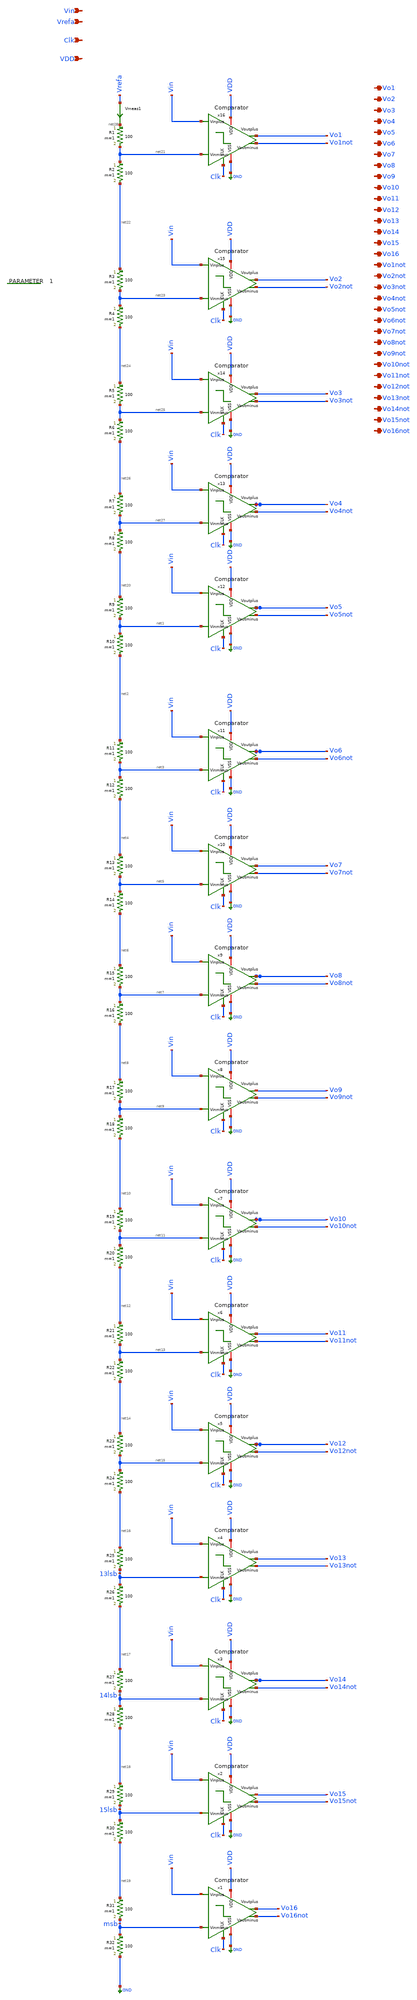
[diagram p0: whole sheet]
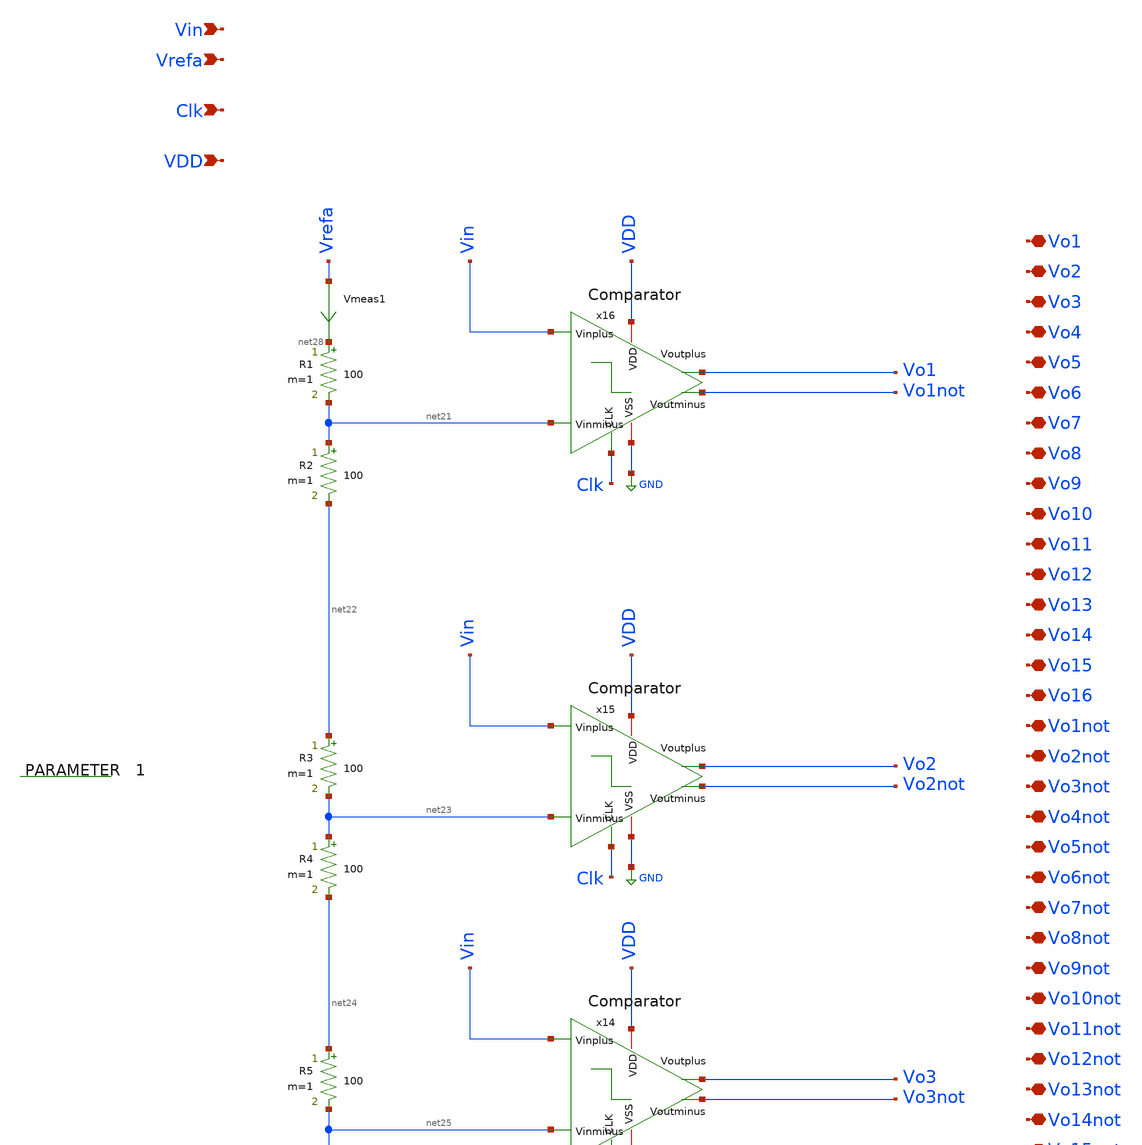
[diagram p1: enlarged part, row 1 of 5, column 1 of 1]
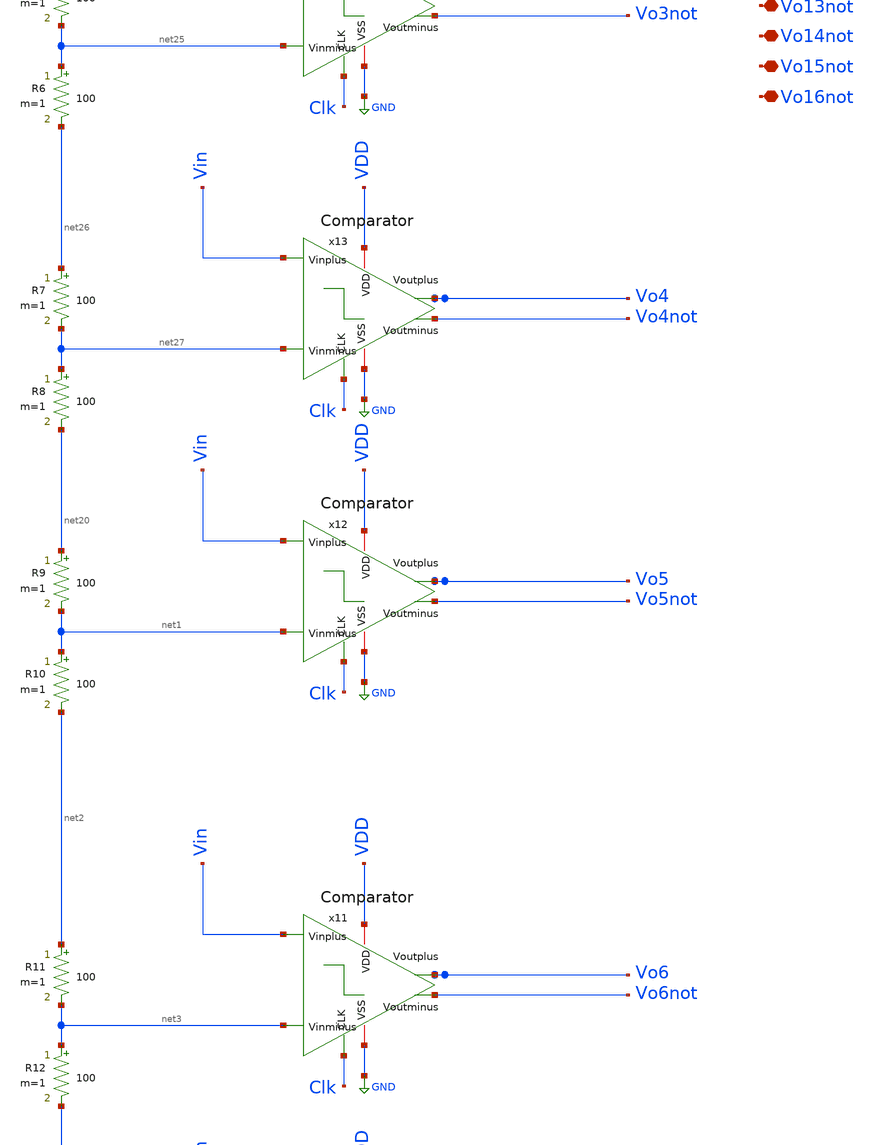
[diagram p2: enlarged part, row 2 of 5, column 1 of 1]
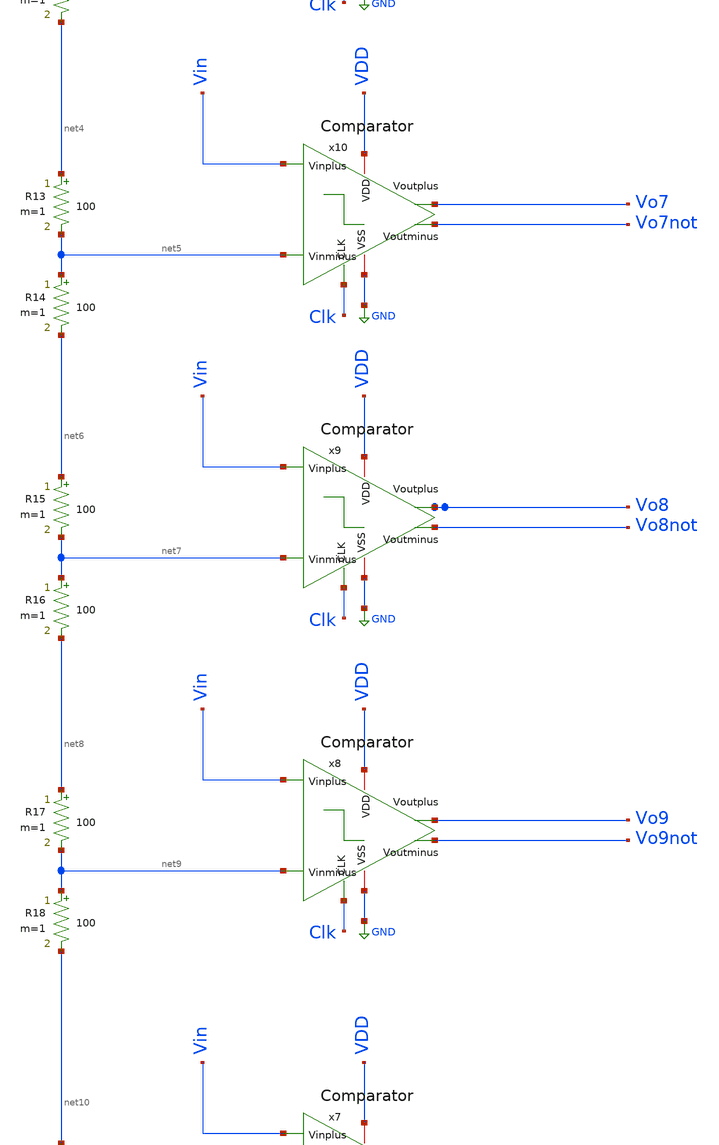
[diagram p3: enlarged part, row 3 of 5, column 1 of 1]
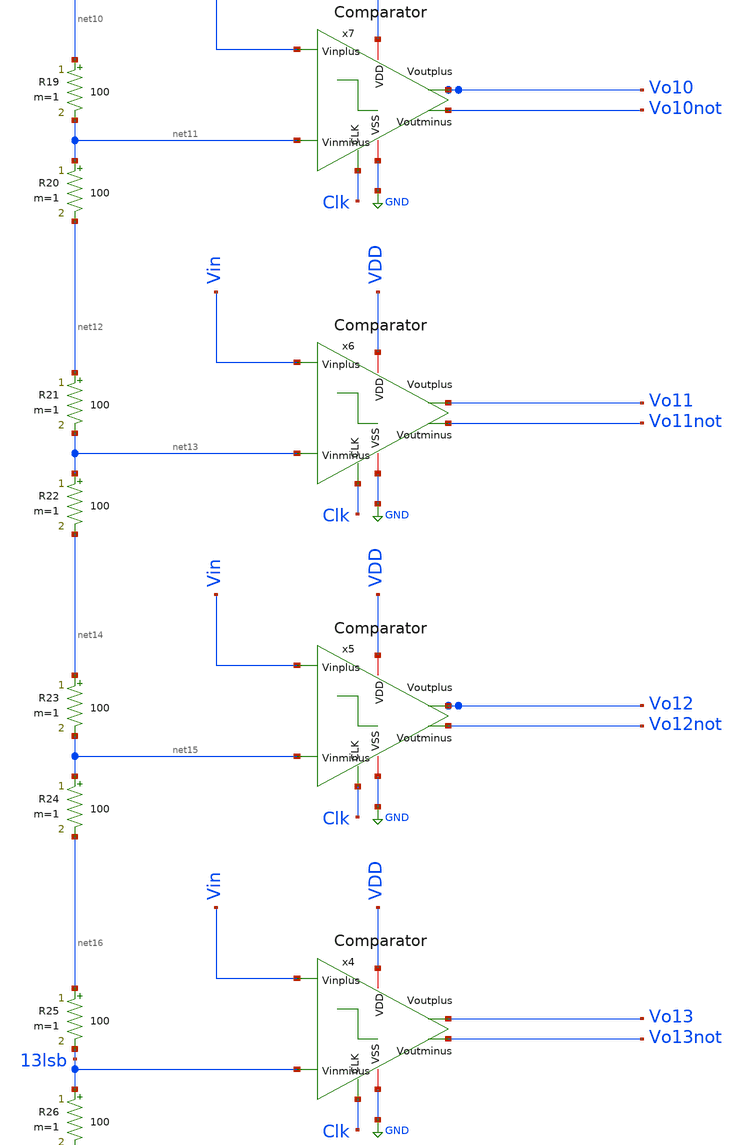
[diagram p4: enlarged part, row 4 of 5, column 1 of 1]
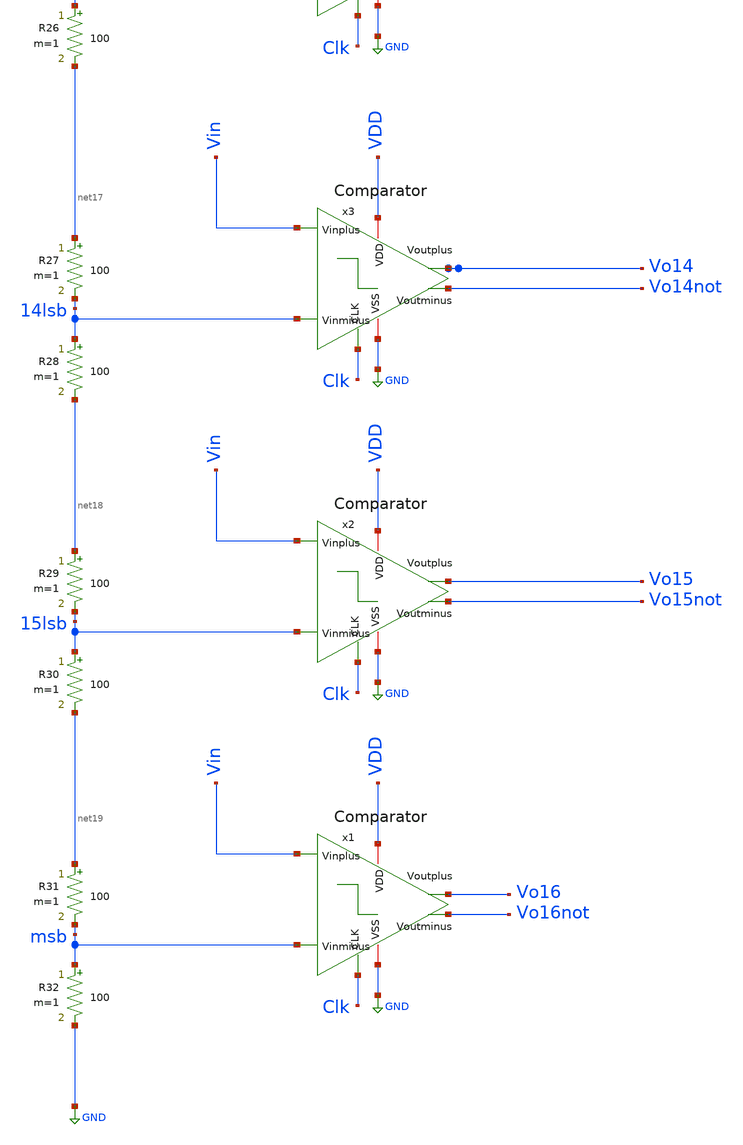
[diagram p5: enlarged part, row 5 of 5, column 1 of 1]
** sch_path: xschem/to_send/4bitADC.sch
**.subckt 4bitADC Vin Vrefa Clk VDD Vo1 Vo2 Vo3 Vo4 Vo5 Vo6 Vo7 Vo8 Vo9 Vo10 Vo11 Vo12 Vo13 Vo14
*+ Vo16 Vo16not Vo14not Vo13not Vo12not Vo11not Vo10not Vo9not Vo8not Vo7not Vo6not Vo5not Vo4not Vo3not
*+ Vo2not Vo1not Vo15 Vo15not
*.ipin Vin
*.ipin Vrefa
*.ipin Clk
*.ipin VDD
*.iopin Vo1
*.iopin Vo2
*.iopin Vo3
*.iopin Vo4
*.iopin Vo5
*.iopin Vo6
*.iopin Vo7
*.iopin Vo8
*.iopin Vo9
*.iopin Vo10
*.iopin Vo11
*.iopin Vo12
*.iopin Vo13
*.iopin Vo14
*.iopin Vo16
*.iopin Vo16not
*.iopin Vo14not
*.iopin Vo13not
*.iopin Vo12not
*.iopin Vo11not
*.iopin Vo10not
*.iopin Vo9not
*.iopin Vo8not
*.iopin Vo7not
*.iopin Vo6not
*.iopin Vo5not
*.iopin Vo4not
*.iopin Vo3not
*.iopin Vo2not
*.iopin Vo1not
*.iopin Vo15
*.iopin Vo15not
Vmeas1 Vrefa net28 0
.save i(vmeas1)
R1 net28 net21 100 m=1
R2 net21 net22 100 m=1
R3 net22 net23 100 m=1
R4 net23 net24 100 m=1
R5 net24 net25 100 m=1
R6 net25 net26 100 m=1
R7 net26 net27 100 m=1
R8 net27 net20 100 m=1
R9 net20 net1 100 m=1
R10 net1 net2 100 m=1
R11 net2 net3 100 m=1
R12 net3 net4 100 m=1
R13 net4 net5 100 m=1
R14 net5 net6 100 m=1
R15 net6 net7 100 m=1
R16 net7 net8 100 m=1
R17 net8 net9 100 m=1
R18 net9 net10 100 m=1
R19 net10 net11 100 m=1
R20 net11 net12 100 m=1
R21 net12 net13 100 m=1
R22 net13 net14 100 m=1
R23 net14 net15 100 m=1
R24 net15 net16 100 m=1
R25 net16 13lsb 100 m=1
R26 13lsb net17 100 m=1
R27 net17 14lsb 100 m=1
R28 14lsb net18 100 m=1
R29 net18 15lsb 100 m=1
R30 15lsb net19 100 m=1
R31 net19 msb 100 m=1
R32 msb GND 100 m=1
.param 1
x1 VDD Vo16not Vo16 Clk Vin msb GND Comparator
x2 VDD Vo15not Vo15 Clk Vin 15lsb GND Comparator
x3 VDD Vo14not Vo14 Clk Vin 14lsb GND Comparator
x4 VDD Vo13not Vo13 Clk Vin 13lsb GND Comparator
x5 VDD Vo12not Vo12 Clk Vin net15 GND Comparator
x6 VDD Vo11not Vo11 Clk Vin net13 GND Comparator
x7 VDD Vo10not Vo10 Clk Vin net11 GND Comparator
x8 VDD Vo9not Vo9 Clk Vin net9 GND Comparator
x9 VDD Vo8not Vo8 Clk Vin net7 GND Comparator
x10 VDD Vo7not Vo7 Clk Vin net5 GND Comparator
x11 VDD Vo6not Vo6 Clk Vin net3 GND Comparator
x12 VDD Vo5not Vo5 Clk Vin net1 GND Comparator
x13 VDD Vo4not Vo4 Clk Vin net27 GND Comparator
x14 VDD Vo3not Vo3 Clk Vin net25 GND Comparator
x15 VDD Vo2not Vo2 Clk Vin net23 GND Comparator
x16 VDD Vo1not Vo1 Clk Vin net21 GND Comparator
**.ends
.GLOBAL GND
.end
